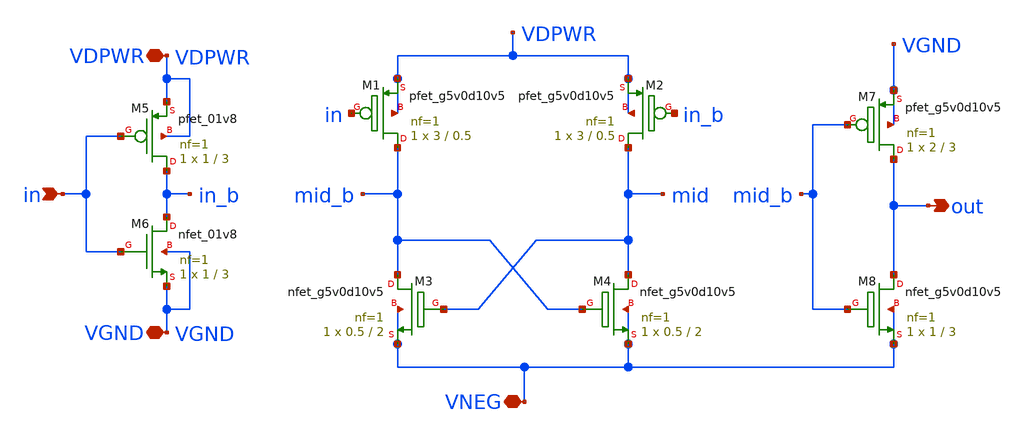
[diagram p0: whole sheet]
** sch_path: xschem/level_shifter_neg.sch
**.subckt level_shifter_neg VNEG VDPWR in VGND out
*.iopin VNEG
*.iopin VDPWR
*.ipin in
*.iopin VGND
*.opin out
XM6 in_b in VGND VGND sky130_fd_pr__nfet_01v8 L=3 W=1 nf=1 ad='int((nf+1)/2) * W/nf * 0.29' as='int((nf+2)/2) * W/nf * 0.29'
+ pd='2*int((nf+1)/2) * (W/nf + 0.29)' ps='2*int((nf+2)/2) * (W/nf + 0.29)' nrd='0.29 / W' nrs='0.29 / W'
+ sa=0 sb=0 sd=0 mult=1 m=1
XM5 in_b in VDPWR VDPWR sky130_fd_pr__pfet_01v8 L=3 W=1 nf=1 ad='int((nf+1)/2) * W/nf * 0.29' as='int((nf+2)/2) * W/nf * 0.29'
+ pd='2*int((nf+1)/2) * (W/nf + 0.29)' ps='2*int((nf+2)/2) * (W/nf + 0.29)' nrd='0.29 / W' nrs='0.29 / W'
+ sa=0 sb=0 sd=0 mult=1 m=1
XM1 mid_b in VDPWR VDPWR sky130_fd_pr__pfet_g5v0d10v5 L=0.5 W=3 nf=1 ad='int((nf+1)/2) * W/nf * 0.29'
+ as='int((nf+2)/2) * W/nf * 0.29' pd='2*int((nf+1)/2) * (W/nf + 0.29)' ps='2*int((nf+2)/2) * (W/nf + 0.29)'
+ nrd='0.29 / W' nrs='0.29 / W' sa=0 sb=0 sd=0 mult=1 m=1
XM2 mid in_b VDPWR VDPWR sky130_fd_pr__pfet_g5v0d10v5 L=0.5 W=3 nf=1 ad='int((nf+1)/2) * W/nf * 0.29'
+ as='int((nf+2)/2) * W/nf * 0.29' pd='2*int((nf+1)/2) * (W/nf + 0.29)' ps='2*int((nf+2)/2) * (W/nf + 0.29)'
+ nrd='0.29 / W' nrs='0.29 / W' sa=0 sb=0 sd=0 mult=1 m=1
XM4 mid mid_b VNEG VNEG sky130_fd_pr__nfet_g5v0d10v5 L=2 W=0.5 nf=1 ad='int((nf+1)/2) * W/nf * 0.29'
+ as='int((nf+2)/2) * W/nf * 0.29' pd='2*int((nf+1)/2) * (W/nf + 0.29)' ps='2*int((nf+2)/2) * (W/nf + 0.29)'
+ nrd='0.29 / W' nrs='0.29 / W' sa=0 sb=0 sd=0 mult=1 m=1
XM3 mid_b mid VNEG VNEG sky130_fd_pr__nfet_g5v0d10v5 L=2 W=0.5 nf=1 ad='int((nf+1)/2) * W/nf * 0.29'
+ as='int((nf+2)/2) * W/nf * 0.29' pd='2*int((nf+1)/2) * (W/nf + 0.29)' ps='2*int((nf+2)/2) * (W/nf + 0.29)'
+ nrd='0.29 / W' nrs='0.29 / W' sa=0 sb=0 sd=0 mult=1 m=1
XM7 out mid_b VGND VGND sky130_fd_pr__pfet_g5v0d10v5 L=3 W=2 nf=1 ad='int((nf+1)/2) * W/nf * 0.29' as='int((nf+2)/2) * W/nf * 0.29'
+ pd='2*int((nf+1)/2) * (W/nf + 0.29)' ps='2*int((nf+2)/2) * (W/nf + 0.29)' nrd='0.29 / W' nrs='0.29 / W'
+ sa=0 sb=0 sd=0 mult=1 m=1
XM8 out mid_b VNEG VNEG sky130_fd_pr__nfet_g5v0d10v5 L=3 W=1 nf=1 ad='int((nf+1)/2) * W/nf * 0.29' as='int((nf+2)/2) * W/nf * 0.29'
+ pd='2*int((nf+1)/2) * (W/nf + 0.29)' ps='2*int((nf+2)/2) * (W/nf + 0.29)' nrd='0.29 / W' nrs='0.29 / W'
+ sa=0 sb=0 sd=0 mult=1 m=1
**.ends
.end
